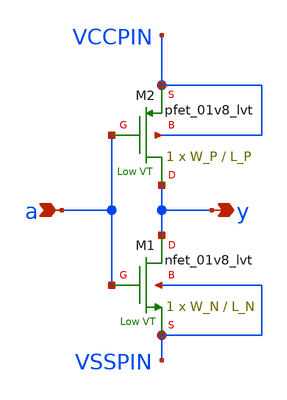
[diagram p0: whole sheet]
** sch_path: sky130_tests/lvtnot.sch
**.subckt lvtnot y a
*.opin y
*.ipin a
XM1 y a VSSPIN VSSPIN sky130_fd_pr__nfet_01v8_lvt W=W_N L=L_N ad='W * 0.29' pd='W + 2 * 0.29' as='W * 0.29'
+ ps='W + 2 * 0.29' nrd=0 nrs=0 sa=0 sb=0 sd=0 nf=1 mult=1
XM2 y a VCCPIN VCCPIN sky130_fd_pr__pfet_01v8_lvt W=W_P L=L_P ad='W * 0.29' pd='W + 2 * 0.29' as='W * 0.29'
+ ps='W + 2 * 0.29' nrd=0 nrs=0 sa=0 sb=0 sd=0 nf=1 mult=1
**.ends
.end
